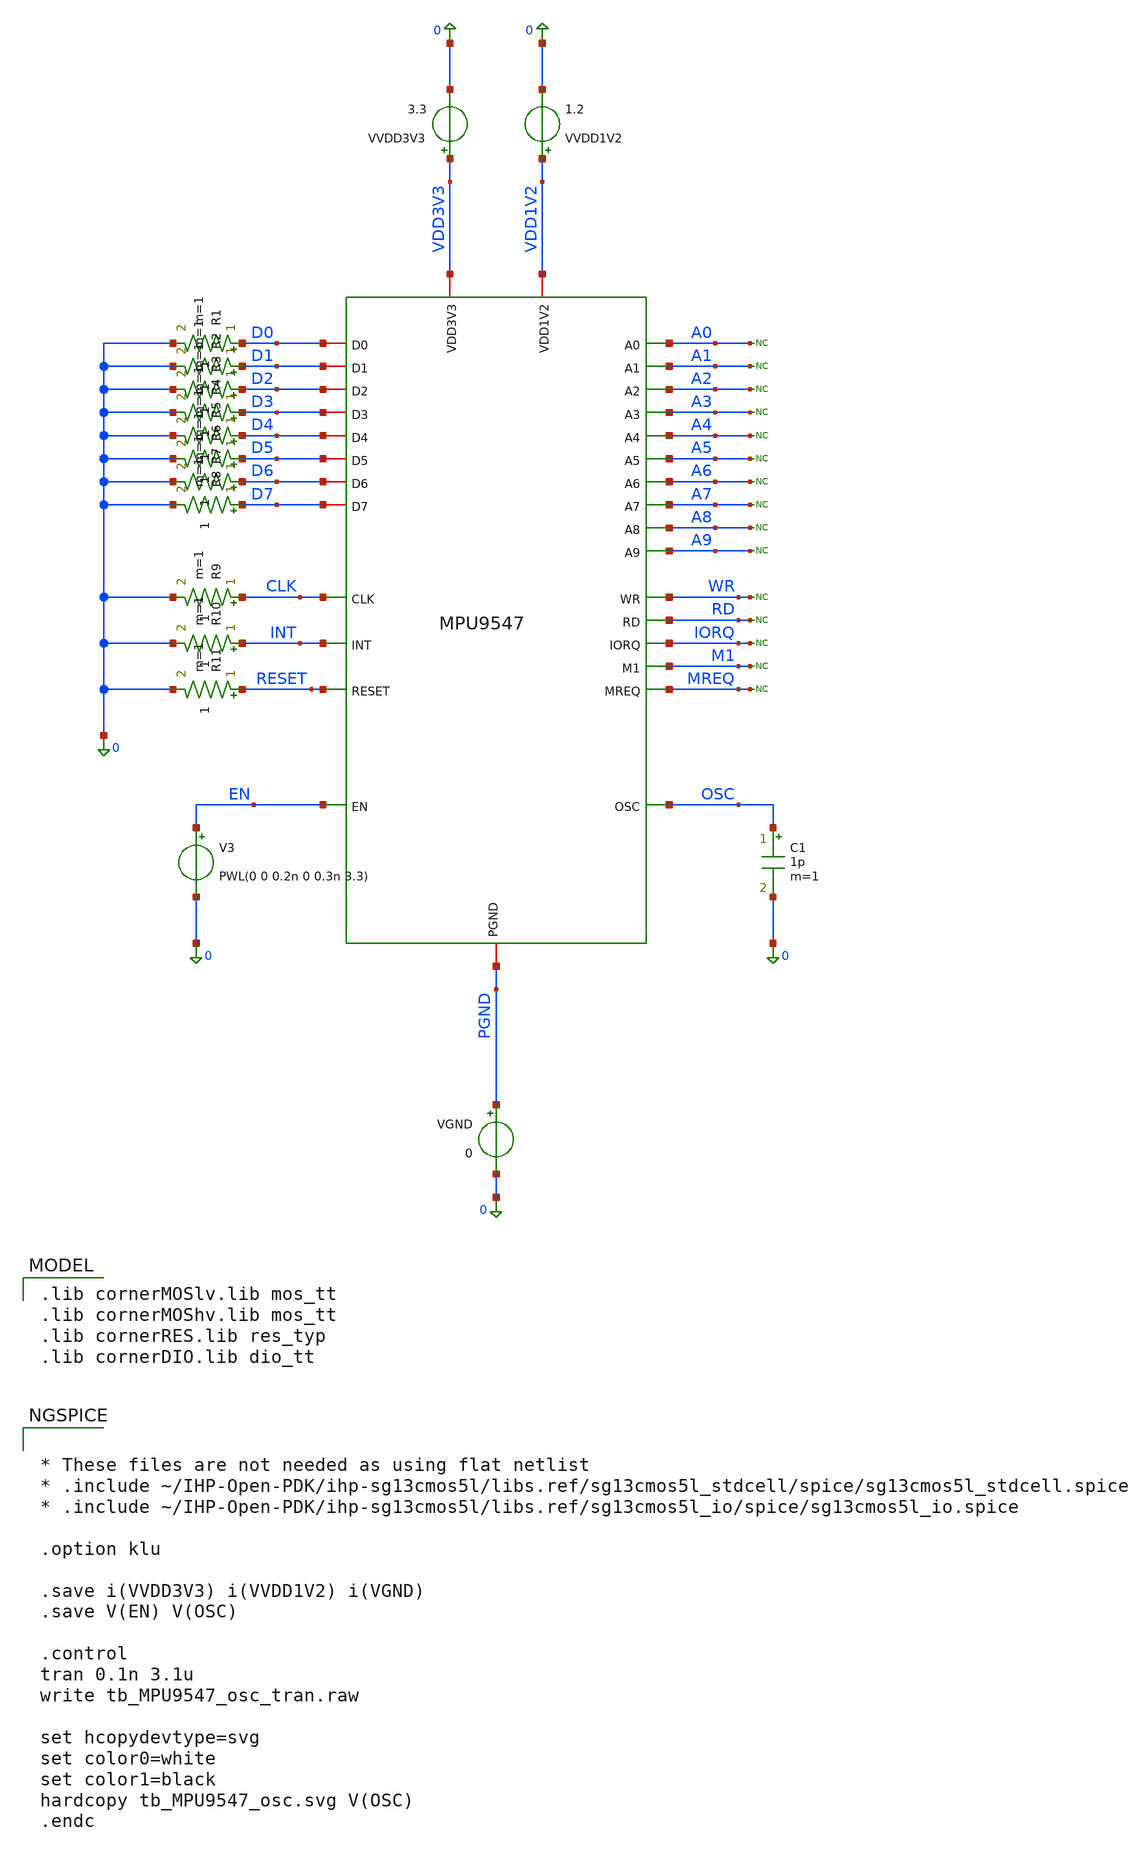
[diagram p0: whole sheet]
** sch_path: MPU9547-main/analog/schematic/tb_MPU9547_osc_tran.sch
**.subckt tb_MPU9547_osc_tran
VVDD3V3 VDD3V3 0 3.3
.save i(vvdd3v3)
VVDD1V2 VDD1V2 0 1.2
.save i(vvdd1v2)
V3 EN 0 PWL(0 0 0.2n 0 0.3n 3.3)
* noconn A0
* noconn A1
* noconn A2
* noconn A3
* noconn A4
* noconn A5
* noconn A6
* noconn A7
* noconn A8
* noconn A9
* noconn WR
* noconn RD
* noconn IORQ
* noconn M1
* noconn MREQ
C1 OSC 0 1p m=1
x1 A4 A5 A6 VDD3V3 PGND A7 A8 A9 IORQ M1 RESET OSC EN CLK INT MREQ WR RD D7 VDD1V2 D6 D5 D4 D3 D2 D1
+ D0 A0 A1 A2 A3 MPU9547
R1 D0 0 1 m=1
R2 D1 0 1 m=1
R3 D2 0 1 m=1
R4 D3 0 1 m=1
R5 D4 0 1 m=1
R6 D5 0 1 m=1
R7 D6 0 1 m=1
R8 D7 0 1 m=1
R9 CLK 0 1 m=1
R10 INT 0 1 m=1
R11 RESET 0 1 m=1
VGND PGND 0 0
.save i(vgnd)
**** begin user architecture code
 .lib cornerMOSlv.lib mos_tt
.lib cornerMOShv.lib mos_tt
.lib cornerRES.lib res_typ
.lib cornerDIO.lib dio_tt



* These files are not needed as using flat netlist
* .include ~/IHP-Open-PDK/ihp-sg13cmos5l/libs.ref/sg13cmos5l_stdcell/spice/sg13cmos5l_stdcell.spice
* .include ~/IHP-Open-PDK/ihp-sg13cmos5l/libs.ref/sg13cmos5l_io/spice/sg13cmos5l_io.spice

.option klu

.save i(VVDD3V3) i(VVDD1V2) i(VGND)
.save V(EN) V(OSC)

.control
tran 0.1n 3.1u
write tb_MPU9547_osc_tran.raw

set hcopydevtype=svg
set color0=white
set color1=black
hardcopy tb_MPU9547_osc.svg V(OSC)
.endc



**** end user architecture code
**.ends

* expanding   symbol:  MPU9547.sym # of pins=31
** sym_path: MPU9547-main/analog/schematic/MPU9547.sym
.include /home/lowneyd/projects/mandalore/analog/schematic/simulation/MPU9547_extracted.cir
.end
